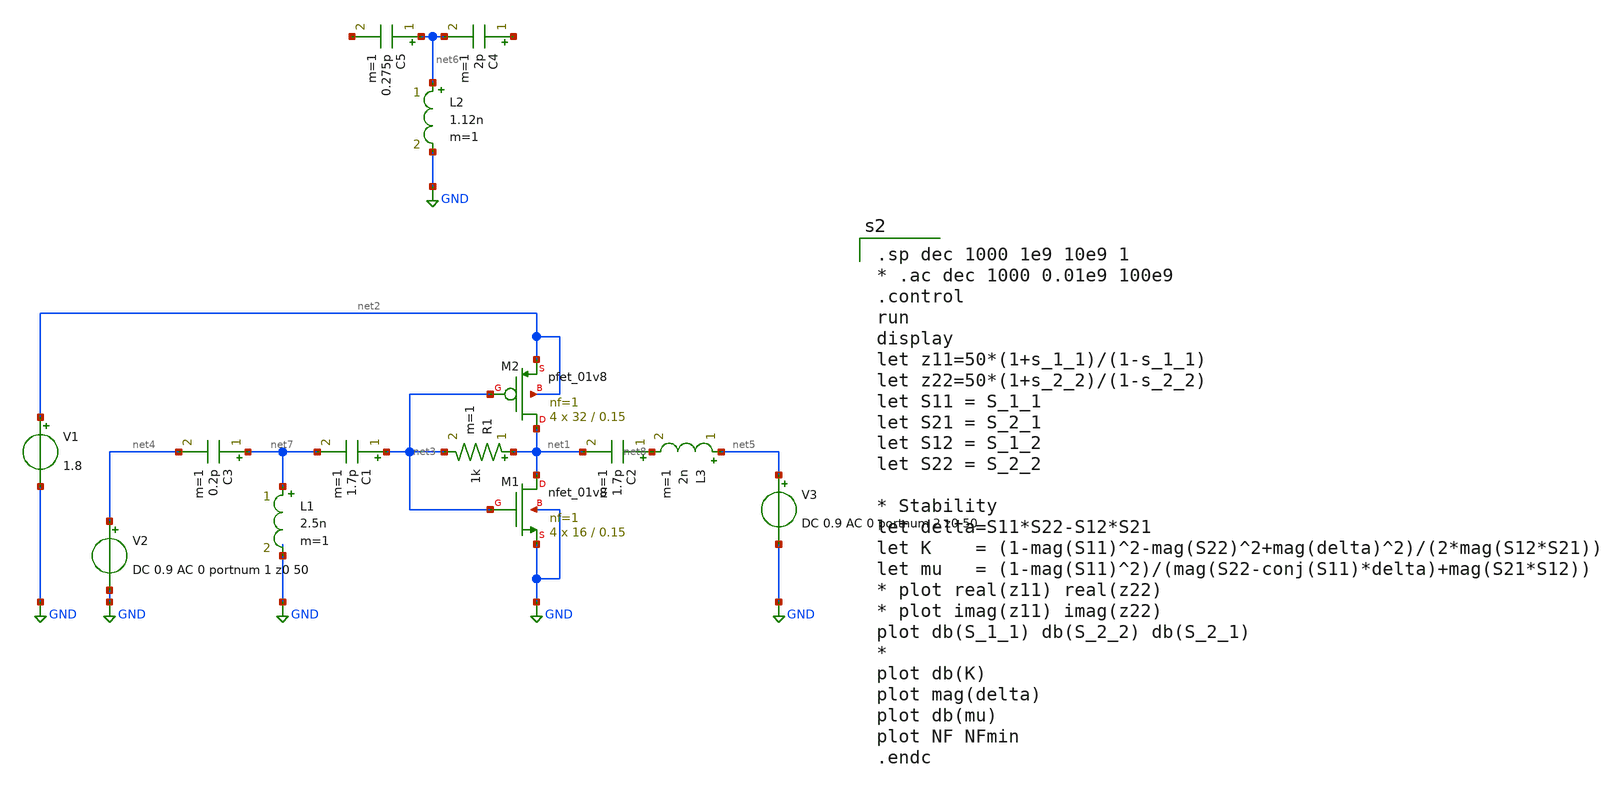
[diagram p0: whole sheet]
** sch_path: xschem/dumb_amp_1.sch
**.subckt dumb_amp_1
XM1 net1 net3 GND GND sky130_fd_pr__nfet_01v8 L=0.15 W=16 nf=1 ad='int((nf+1)/2) * W/nf * 0.29' as='int((nf+2)/2) * W/nf * 0.29'
+ pd='2*int((nf+1)/2) * (W/nf + 0.29)' ps='2*int((nf+2)/2) * (W/nf + 0.29)' nrd='0.29 / W' nrs='0.29 / W'
+ sa=0 sb=0 sd=0 mult=4 m=4
XM2 net1 net3 net2 net2 sky130_fd_pr__pfet_01v8 L=0.15 W=32 nf=1 ad='int((nf+1)/2) * W/nf * 0.29' as='int((nf+2)/2) * W/nf * 0.29'
+ pd='2*int((nf+1)/2) * (W/nf + 0.29)' ps='2*int((nf+2)/2) * (W/nf + 0.29)' nrd='0.29 / W' nrs='0.29 / W'
+ sa=0 sb=0 sd=0 mult=4 m=4
V1 net2 GND 1.8
R1 net1 net3 1k m=1
V3 net5 GND DC 0.9 AC 0 portnum 2 z0 50
V2 net4 GND DC 0.9 AC 0 portnum 1 z0 50
C1 net3 net7 1.7p m=1
C2 net8 net1 1.7p m=1
C4 net9 net6 2p m=1
C5 net6 net10 0.275p m=1
L2 net6 GND 1.12n m=1
C3 net7 net4 0.2p m=1
L1 net7 GND 2.5n m=1
L3 net5 net8 2n m=1
**** begin user architecture code
.lib $::SKYWATER_MODELS/sky130.lib.spice tt
* .include $::PDKPATH/libs.ref/sky130_fd_sc_hvl/spice/sky130_fd_sc_hvl.spice


.sp dec 1000 1e9 10e9 1
* .ac dec 1000 0.01e9 100e9
.control
run
display
let z11=50*(1+s_1_1)/(1-s_1_1)
let z22=50*(1+s_2_2)/(1-s_2_2)
let S11 = S_1_1
let S21 = S_2_1
let S12 = S_1_2
let S22 = S_2_2

* Stability
let delta=S11*S22-S12*S21
let K    = (1-mag(S11)^2-mag(S22)^2+mag(delta)^2)/(2*mag(S12*S21))
let mu   = (1-mag(S11)^2)/(mag(S22-conj(S11)*delta)+mag(S21*S12))
* plot real(z11) real(z22)
* plot imag(z11) imag(z22)
plot db(S_1_1) db(S_2_2) db(S_2_1)
*
plot db(K)
plot mag(delta)
plot db(mu)
plot NF NFmin
.endc


**** end user architecture code
**.ends
.GLOBAL GND
.end
